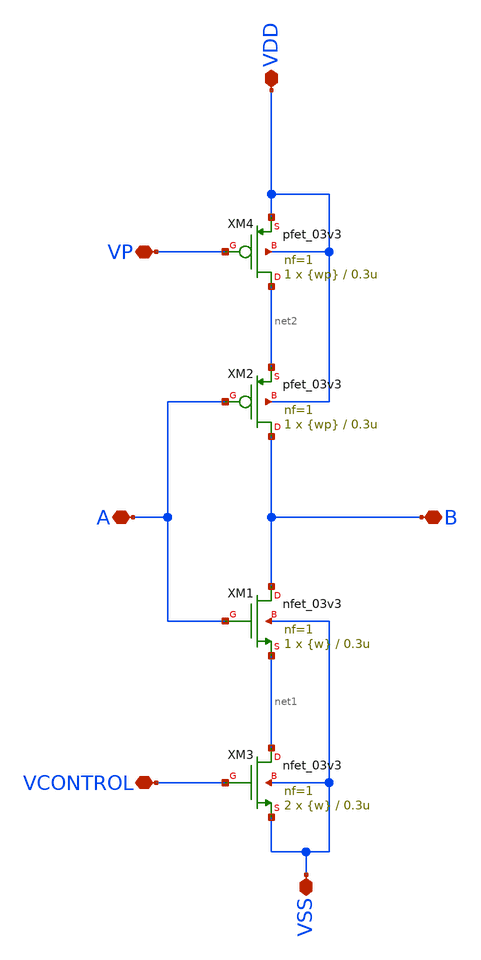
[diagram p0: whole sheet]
** sch_path: designs/ring_oscillator_pg/inversor.sch
**.subckt inversor B A VCONTROL VDD VP VSS
*.iopin B
*.iopin A
*.iopin VCONTROL
*.iopin VDD
*.iopin VP
*.iopin VSS
XM1 B A net1 VSS nfet_03v3 L=0.3u W={w} nf=1 ad='int((nf+1)/2) * W/nf * 0.18u' as='int((nf+2)/2) * W/nf * 0.18u'
+ pd='2*int((nf+1)/2) * (W/nf + 0.18u)' ps='2*int((nf+2)/2) * (W/nf + 0.18u)' nrd='0.18u / W' nrs='0.18u / W'
+ sa=0 sb=0 sd=0 m=1
XM2 B A net2 VDD pfet_03v3 L=0.3u W={wp} nf=1 ad='int((nf+1)/2) * W/nf * 0.18u' as='int((nf+2)/2) * W/nf * 0.18u'
+ pd='2*int((nf+1)/2) * (W/nf + 0.18u)' ps='2*int((nf+2)/2) * (W/nf + 0.18u)' nrd='0.18u / W' nrs='0.18u / W'
+ sa=0 sb=0 sd=0 m=1
XM3 net1 VCONTROL VSS VSS nfet_03v3 L=0.3u W={w} nf=1 ad='int((nf+1)/2) * W/nf * 0.18u' as='int((nf+2)/2) * W/nf * 0.18u'
+ pd='2*int((nf+1)/2) * (W/nf + 0.18u)' ps='2*int((nf+2)/2) * (W/nf + 0.18u)' nrd='0.18u / W' nrs='0.18u / W'
+ sa=0 sb=0 sd=0 m=2
XM4 net2 VP VDD VDD pfet_03v3 L=0.3u W={wp} nf=1 ad='int((nf+1)/2) * W/nf * 0.18u' as='int((nf+2)/2) * W/nf * 0.18u'
+ pd='2*int((nf+1)/2) * (W/nf + 0.18u)' ps='2*int((nf+2)/2) * (W/nf + 0.18u)' nrd='0.18u / W' nrs='0.18u / W'
+ sa=0 sb=0 sd=0 m=1
**.ends
.end
